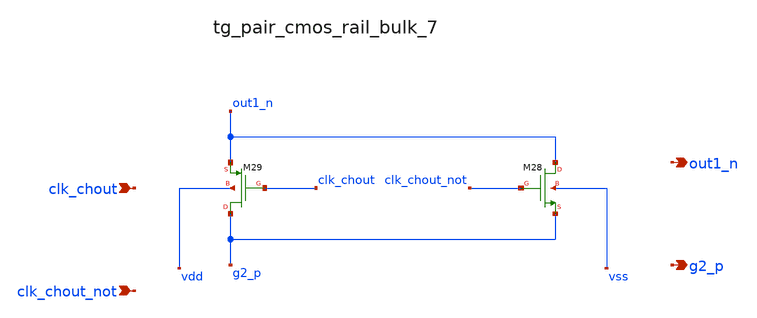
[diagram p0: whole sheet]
** sch_path: analog-db/raw/ia_002_fan_chopper_simple/hier/blocks/tg_pair_cmos_rail_bulk_7.sch
**.subckt tg_pair_cmos_rail_bulk_7 clk_chout clk_chout_not out1_n g2_p
*.ipin clk_chout
*.ipin clk_chout_not
*.opin out1_n
*.opin g2_p
XM28 out1_n clk_chout_not g2_p vss sg13_lv_nmos w=x_dut_xm28_w l=x_dut_xm28_l ng=1 m=x_dut_xm28_m
XM29 g2_p clk_chout out1_n vdd sg13_lv_pmos w=x_dut_xm29_w l=x_dut_xm29_l ng=1 m=x_dut_xm29_m
**.ends
.end
